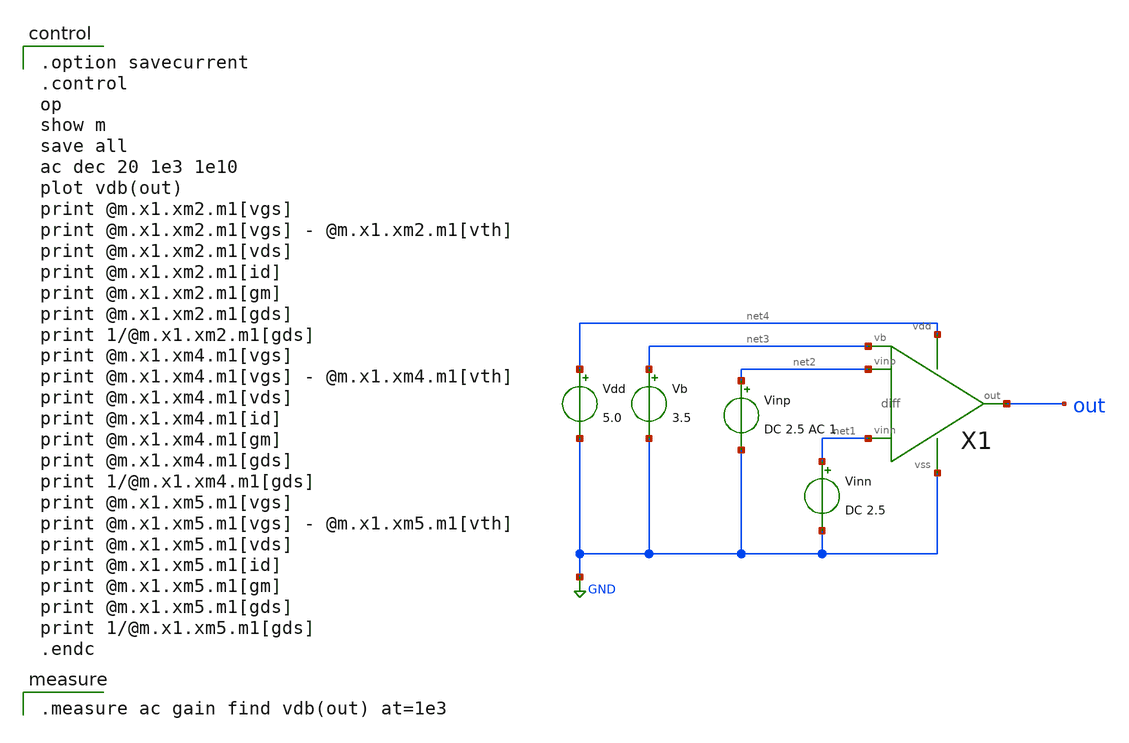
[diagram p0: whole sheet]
** sch_path: OpenSUSI-TR10/opamp/diff_ac.sch
**.subckt diff_ac
Vdd net4 GND 5.0
Vb net3 GND 3.5
Vinn net1 GND DC 2.5
Vinp net2 GND DC 2.5 AC 1
X1 net2 net1 out net4 GND net3 diff
**** begin user architecture code

.option savecurrent
.control
op
show m
save all
ac dec 20 1e3 1e10
plot vdb(out)
print @m.x1.xm2.m1[vgs]
print @m.x1.xm2.m1[vgs] - @m.x1.xm2.m1[vth]
print @m.x1.xm2.m1[vds]
print @m.x1.xm2.m1[id]
print @m.x1.xm2.m1[gm]
print @m.x1.xm2.m1[gds]
print 1/@m.x1.xm2.m1[gds]
print @m.x1.xm4.m1[vgs]
print @m.x1.xm4.m1[vgs] - @m.x1.xm4.m1[vth]
print @m.x1.xm4.m1[vds]
print @m.x1.xm4.m1[id]
print @m.x1.xm4.m1[gm]
print @m.x1.xm4.m1[gds]
print 1/@m.x1.xm4.m1[gds]
print @m.x1.xm5.m1[vgs]
print @m.x1.xm5.m1[vgs] - @m.x1.xm5.m1[vth]
print @m.x1.xm5.m1[vds]
print @m.x1.xm5.m1[id]
print @m.x1.xm5.m1[gm]
print @m.x1.xm5.m1[gds]
print 1/@m.x1.xm5.m1[gds]
.endc


.measure ac gain find vdb(out) at=1e3

 .include $::LIB/ip62_models
**** end user architecture code
**.ends

* expanding   symbol:  diff.sym # of pins=6
** sym_path: diff.sym
** sch_path: diff.sch
.subckt diff vinp vinn out vdd vss vb
*.ipin vinn
*.ipin vinp
*.ipin vb
*.opin out
*.iopin vdd
*.iopin vss
M5 net2 vb vdd vdd pmos L=2u W=40u m=1
M1 net1 vinn net2 net2 pmos L=2u W=200u m=1
M2 out vinp net2 net2 pmos L=2u W=200u m=1
M3 net1 net1 vss vss nmos L=2u W=10u m=1
M4 out net1 vss vss nmos L=2u W=10u m=1
.ends

.GLOBAL GND
.end
